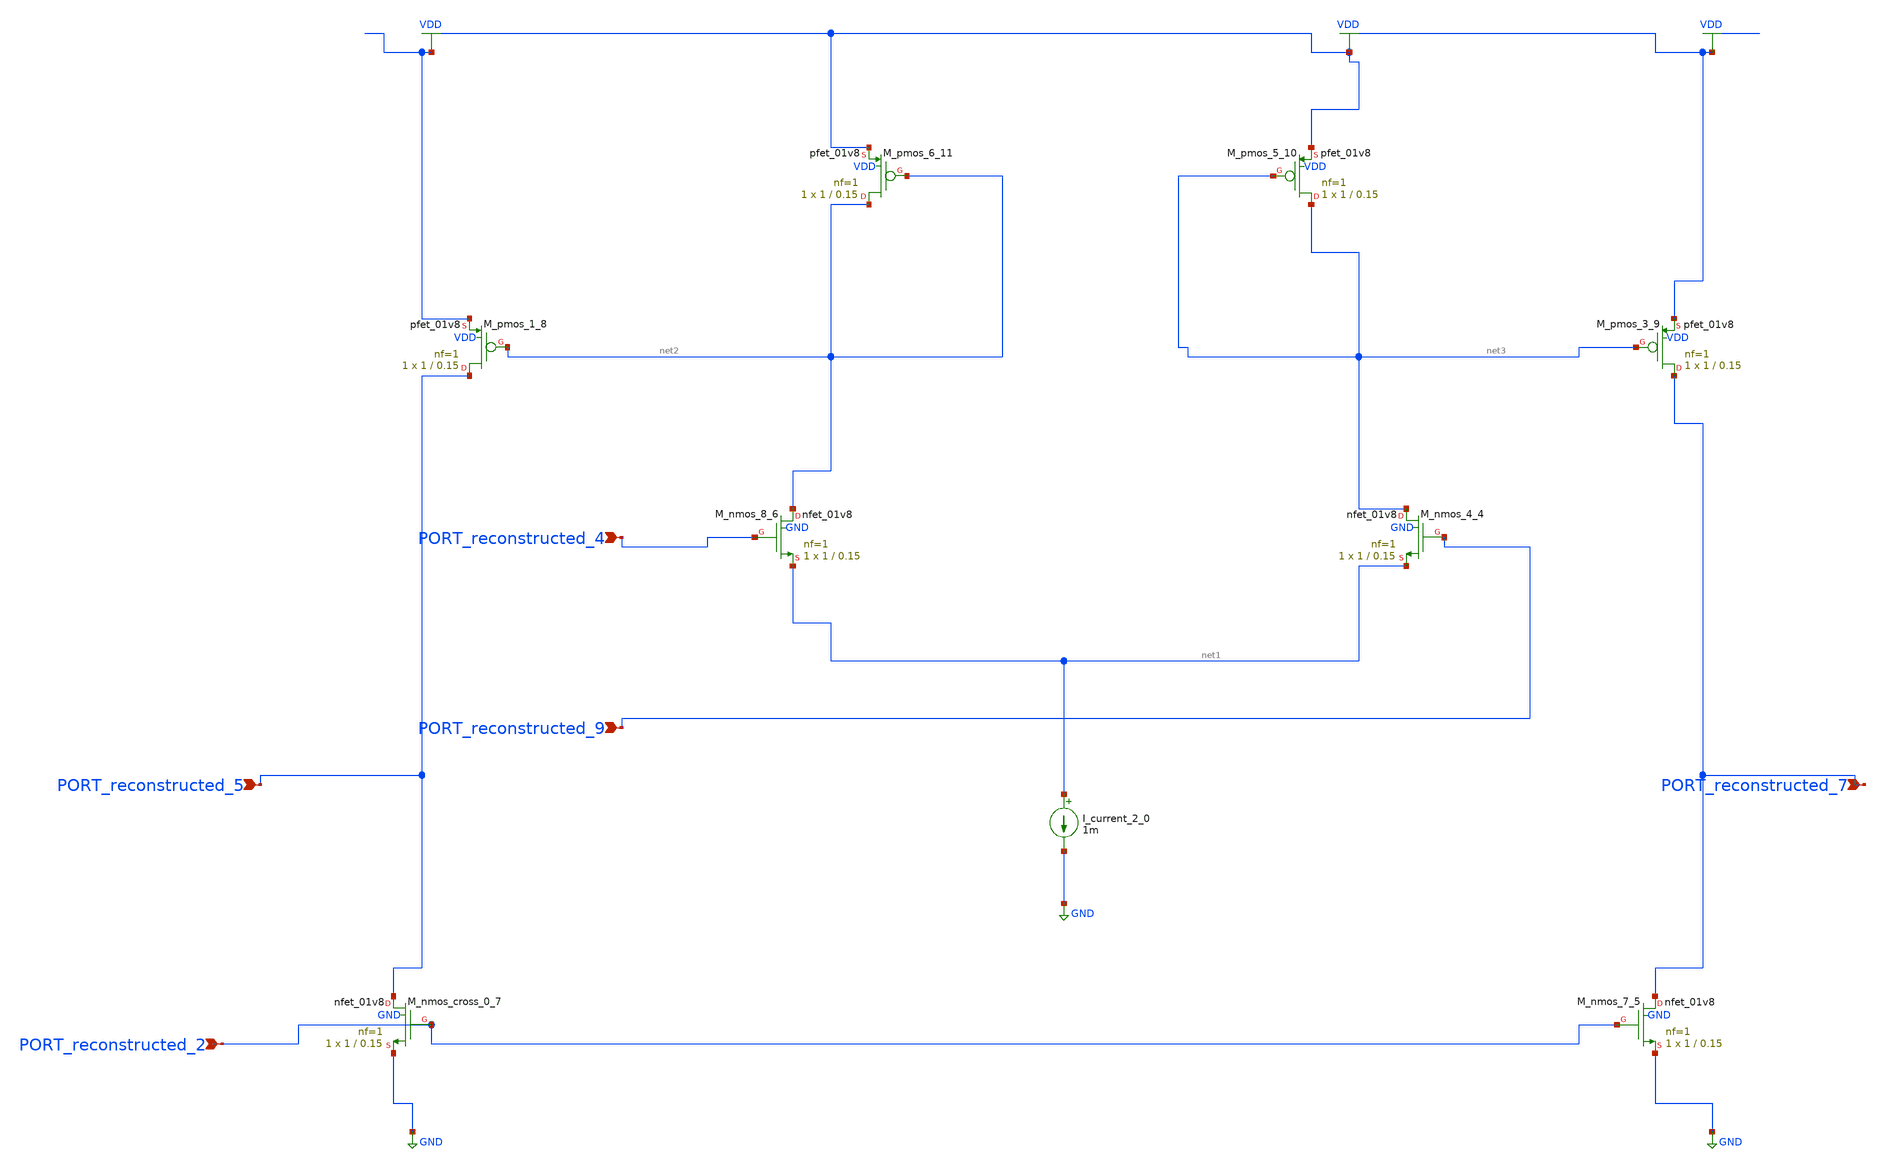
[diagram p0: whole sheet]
** sch_path: schematics/AMSNet/712.sch
**.subckt 712 PORT_reconstructed_4 PORT_reconstructed_7 PORT_reconstructed_5 PORT_reconstructed_9
*+ PORT_reconstructed_2
*.ipin PORT_reconstructed_4
*.ipin PORT_reconstructed_7
*.ipin PORT_reconstructed_5
*.ipin PORT_reconstructed_9
*.ipin PORT_reconstructed_2
I_current_2_0 net1 GND 1m
XM_nmos_4_4 net3 PORT_reconstructed_9 net1 GND sky130_fd_pr__nfet_01v8 L=0.15 W=1 nf=1 ad='int((1 + 1)/2) * 1 / 1 * 0.29'
+ as='int((1 + 2)/2) * 1 / 1 * 0.29' pd='2*int((1 + 1)/2) * (1 / 1 + 0.29)' ps='2*int((1 + 2)/2) * (1 / 1 + 0.29)'
+ nrd='0.29 / 1 ' nrs='0.29 / 1 ' sa=0 sb=0 sd=0 mult=1 m=1
XM_nmos_7_5 PORT_reconstructed_7 PORT_reconstructed_2 GND GND sky130_fd_pr__nfet_01v8 L=0.15 W=1 nf=1
+ ad='int((1 + 1)/2) * 1 / 1 * 0.29' as='int((1 + 2)/2) * 1 / 1 * 0.29' pd='2*int((1 + 1)/2) * (1 / 1 + 0.29)'
+ ps='2*int((1 + 2)/2) * (1 / 1 + 0.29)' nrd='0.29 / 1 ' nrs='0.29 / 1 ' sa=0 sb=0 sd=0 mult=1 m=1
XM_nmos_8_6 net2 PORT_reconstructed_4 net1 GND sky130_fd_pr__nfet_01v8 L=0.15 W=1 nf=1 ad='int((1 + 1)/2) * 1 / 1 * 0.29'
+ as='int((1 + 2)/2) * 1 / 1 * 0.29' pd='2*int((1 + 1)/2) * (1 / 1 + 0.29)' ps='2*int((1 + 2)/2) * (1 / 1 + 0.29)'
+ nrd='0.29 / 1 ' nrs='0.29 / 1 ' sa=0 sb=0 sd=0 mult=1 m=1
XM_nmos_cross_0_7 PORT_reconstructed_5 PORT_reconstructed_2 GND GND sky130_fd_pr__nfet_01v8 L=0.15 W=1
+ nf=1 ad='int((1 + 1)/2) * 1 / 1 * 0.29' as='int((1 + 2)/2) * 1 / 1 * 0.29' pd='2*int((1 + 1)/2) * (1 / 1 + 0.29)'
+ ps='2*int((1 + 2)/2) * (1 / 1 + 0.29)' nrd='0.29 / 1 ' nrs='0.29 / 1 ' sa=0 sb=0 sd=0 mult=1 m=1
XM_pmos_1_8 PORT_reconstructed_5 net2 VDD VDD sky130_fd_pr__pfet_01v8 L=0.15 W=1 nf=1 ad='int((1 + 1)/2) * 1 / 1 * 0.29'
+ as='int((1 + 2)/2) * 1 / 1 * 0.29' pd='2*int((1 + 1)/2) * (1 / 1 + 0.29)' ps='2*int((1 + 2)/2) * (1 / 1 + 0.29)'
+ nrd='0.29 / 1 ' nrs='0.29 / 1 ' sa=0 sb=0 sd=0 mult=1 m=1
XM_pmos_3_9 PORT_reconstructed_7 net3 VDD VDD sky130_fd_pr__pfet_01v8 L=0.15 W=1 nf=1 ad='int((1 + 1)/2) * 1 / 1 * 0.29'
+ as='int((1 + 2)/2) * 1 / 1 * 0.29' pd='2*int((1 + 1)/2) * (1 / 1 + 0.29)' ps='2*int((1 + 2)/2) * (1 / 1 + 0.29)'
+ nrd='0.29 / 1 ' nrs='0.29 / 1 ' sa=0 sb=0 sd=0 mult=1 m=1
XM_pmos_5_10 net3 net3 VDD VDD sky130_fd_pr__pfet_01v8 L=0.15 W=1 nf=1 ad='int((1 + 1)/2) * 1 / 1 * 0.29'
+ as='int((1 + 2)/2) * 1 / 1 * 0.29' pd='2*int((1 + 1)/2) * (1 / 1 + 0.29)' ps='2*int((1 + 2)/2) * (1 / 1 + 0.29)'
+ nrd='0.29 / 1 ' nrs='0.29 / 1 ' sa=0 sb=0 sd=0 mult=1 m=1
XM_pmos_6_11 net2 net2 VDD VDD sky130_fd_pr__pfet_01v8 L=0.15 W=1 nf=1 ad='int((1 + 1)/2) * 1 / 1 * 0.29'
+ as='int((1 + 2)/2) * 1 / 1 * 0.29' pd='2*int((1 + 1)/2) * (1 / 1 + 0.29)' ps='2*int((1 + 2)/2) * (1 / 1 + 0.29)'
+ nrd='0.29 / 1 ' nrs='0.29 / 1 ' sa=0 sb=0 sd=0 mult=1 m=1
**.ends
.GLOBAL GND
.GLOBAL VDD
.end
